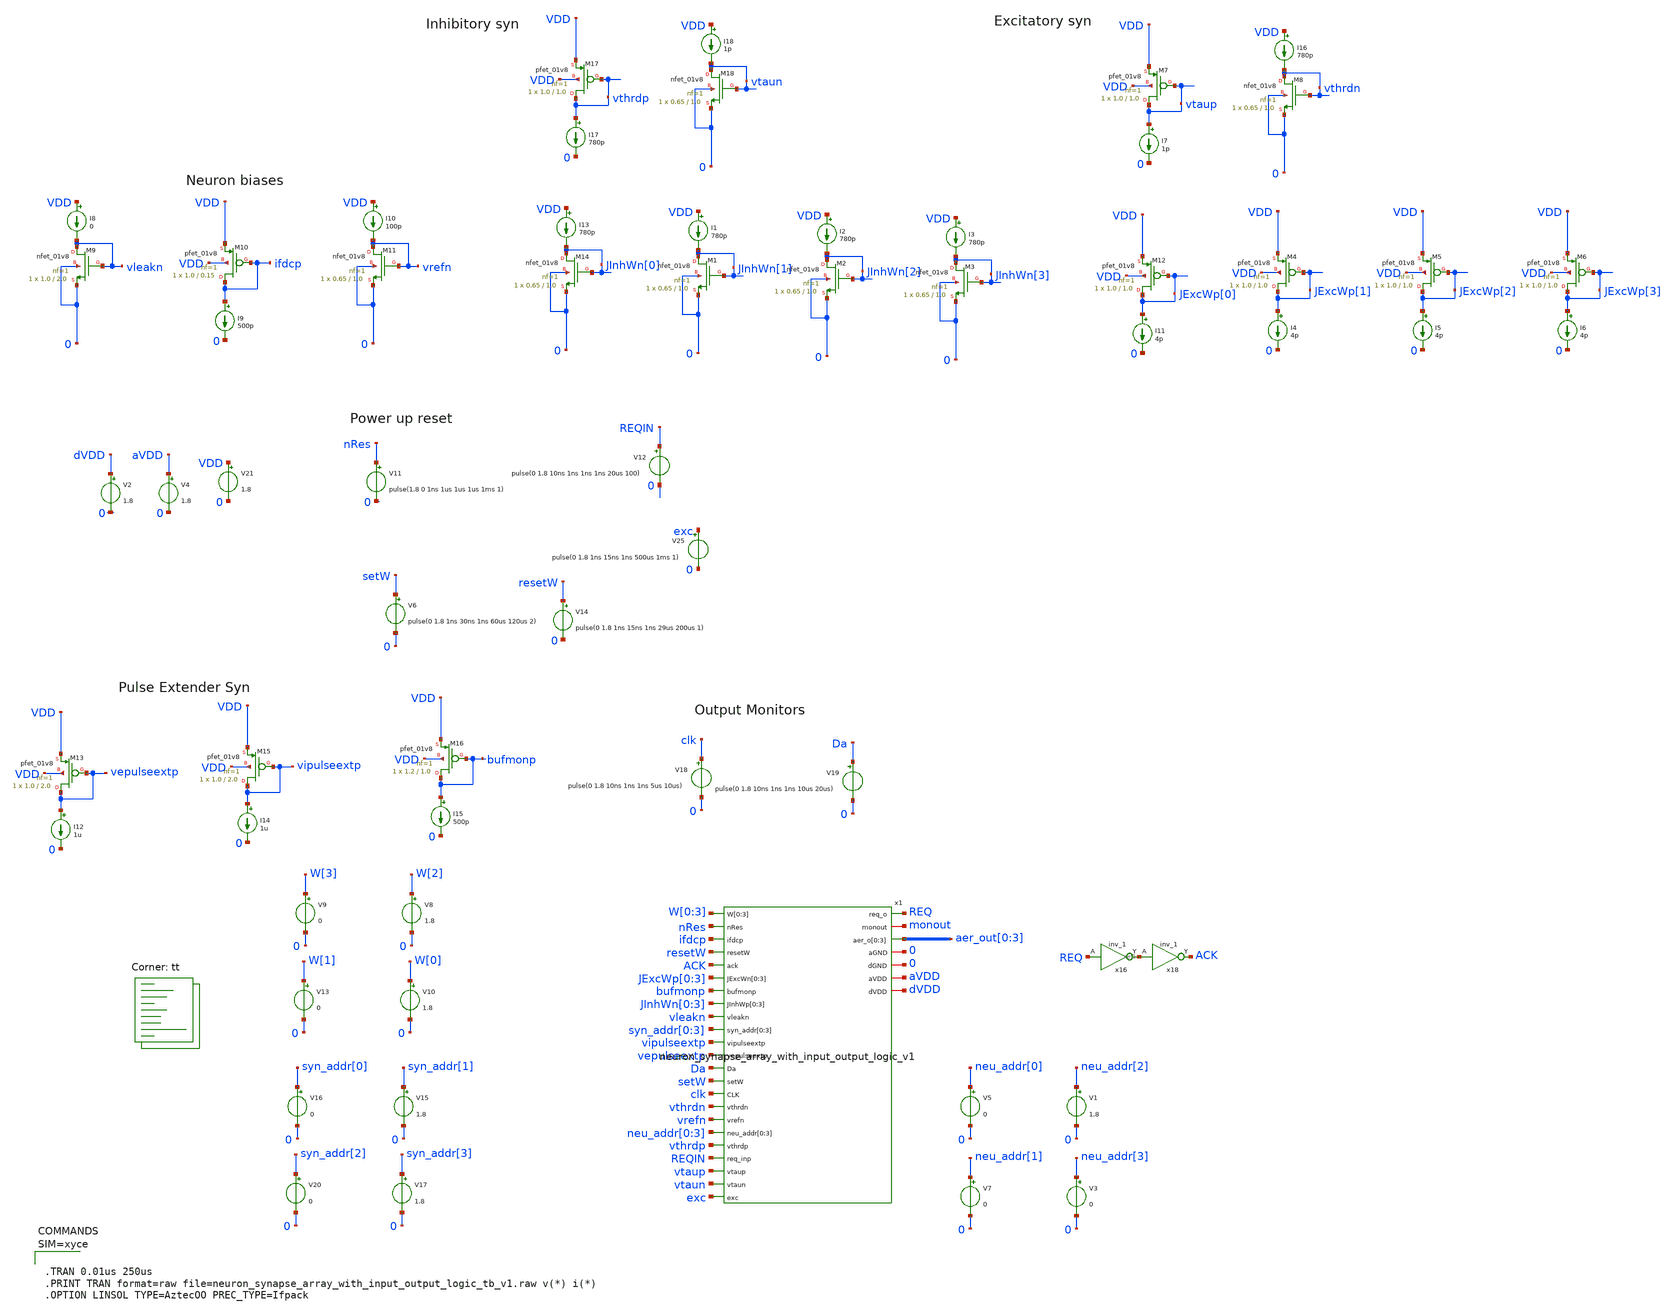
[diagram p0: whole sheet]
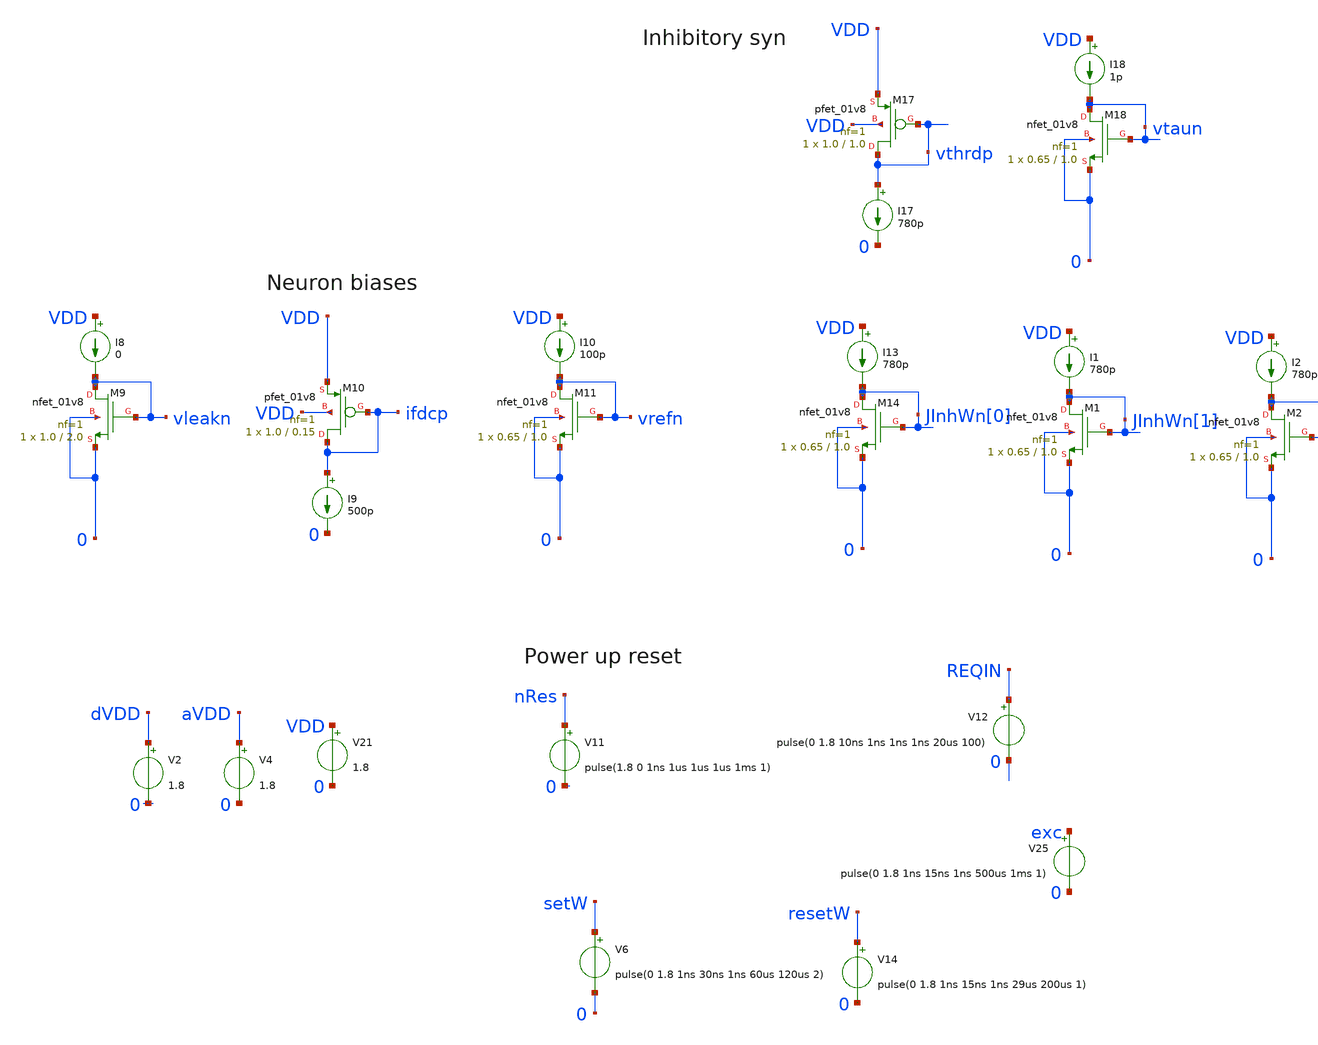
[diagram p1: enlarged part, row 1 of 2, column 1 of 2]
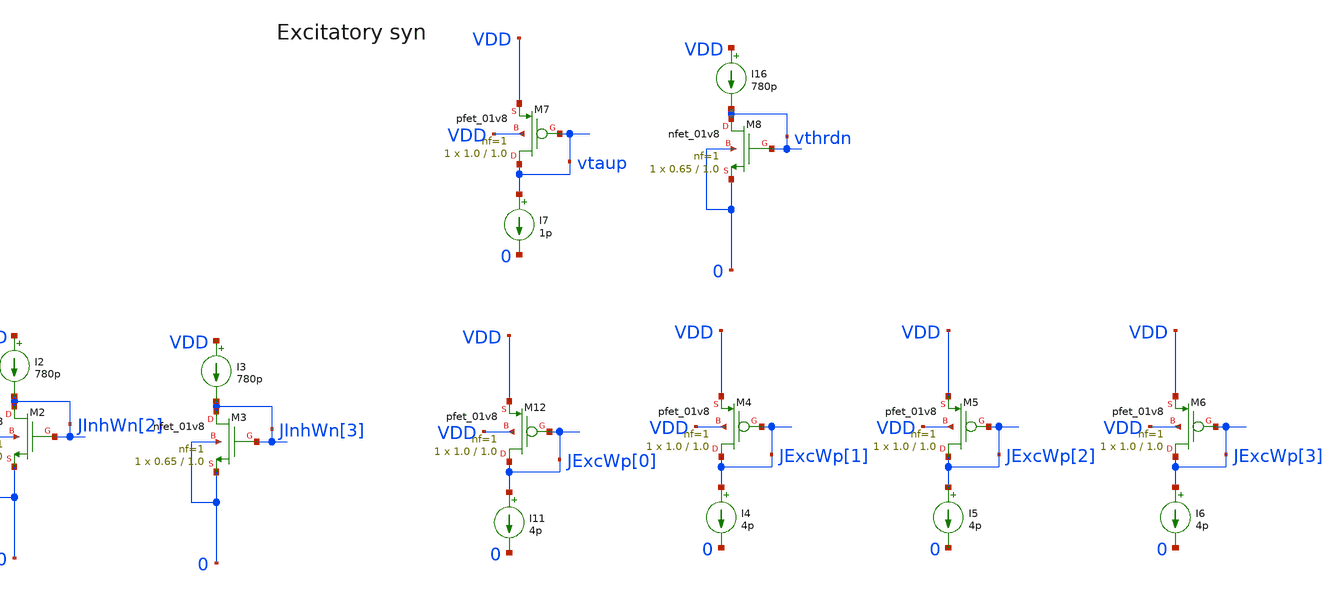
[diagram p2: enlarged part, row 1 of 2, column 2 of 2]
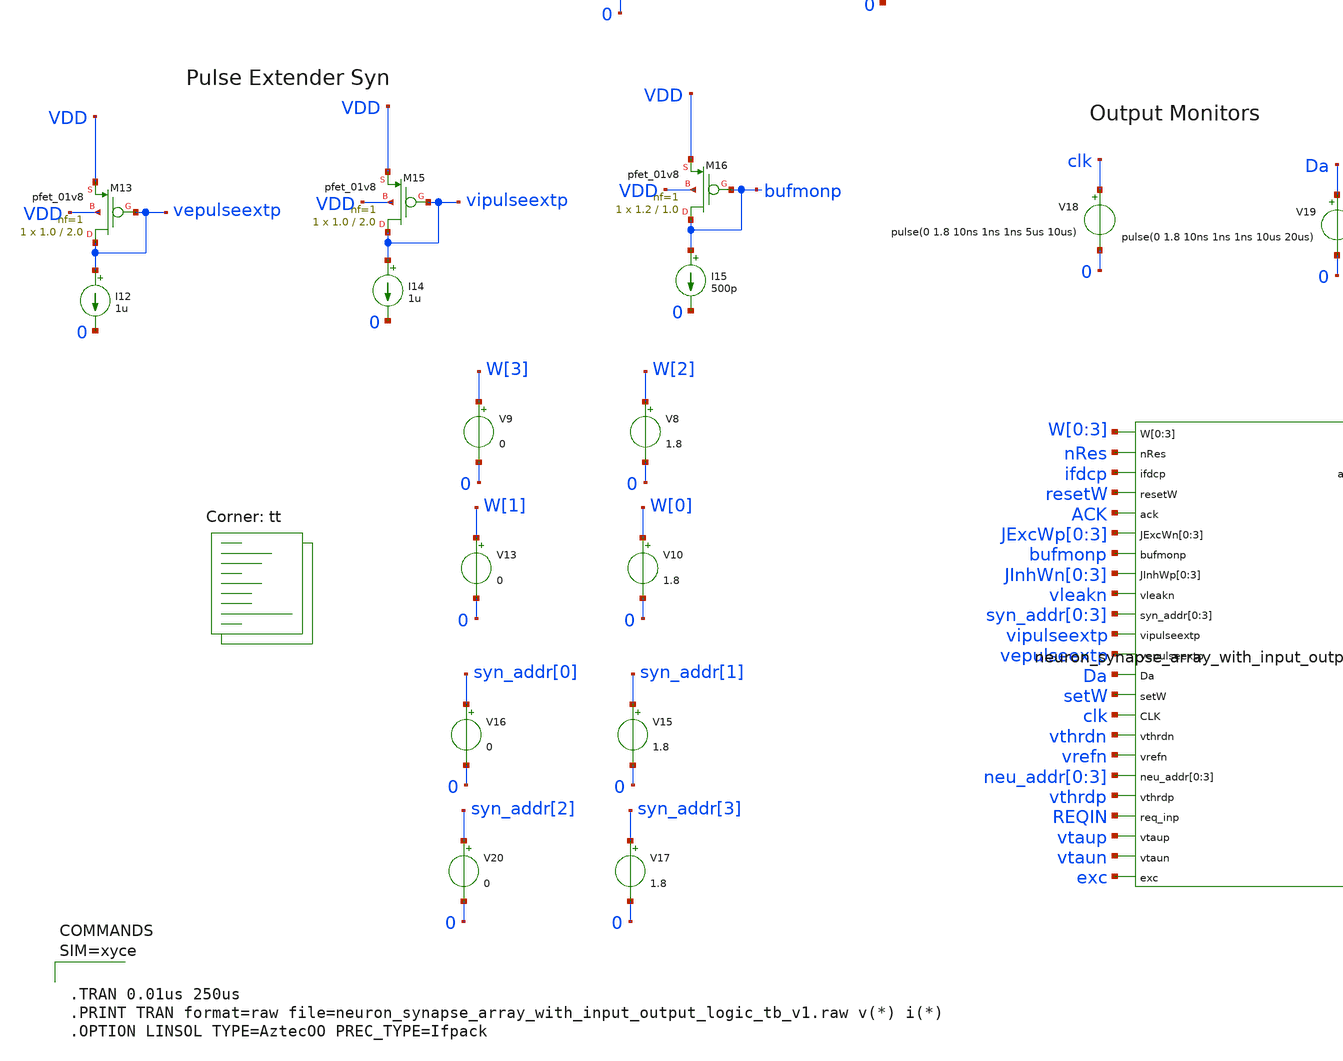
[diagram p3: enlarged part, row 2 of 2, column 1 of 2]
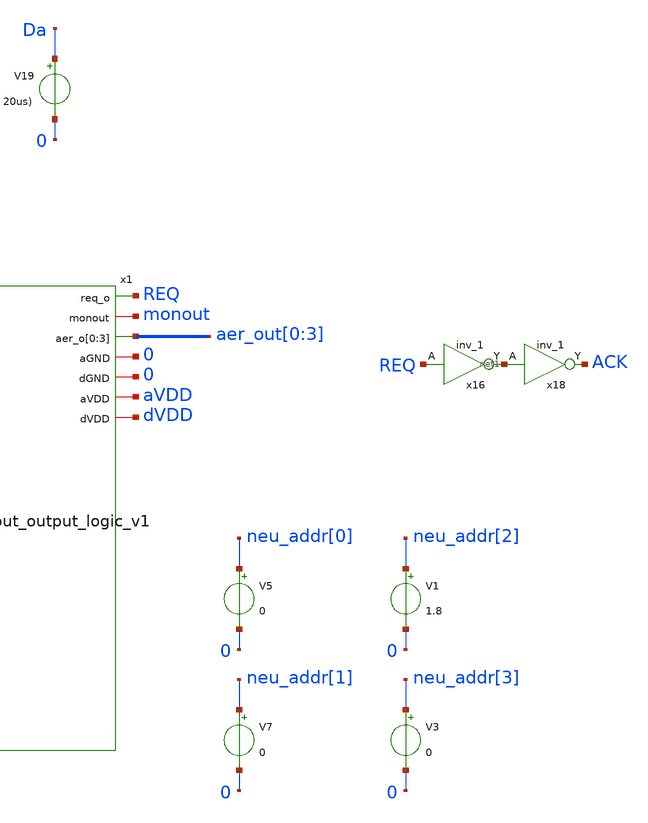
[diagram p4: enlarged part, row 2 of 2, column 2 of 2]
** sch_path: design/xschem/neuron_synapse_array_with_input_output_logic_v1_tb.sch
**.subckt neuron_synapse_array_with_input_output_logic_v1_tb
V2 dVDD 0 1.8
V12 REQIN 0 pulse(0 1.8 10ns 1ns 1ns 1ns 20us 100)
V4 aVDD 0 1.8
V11 nRes 0 pulse(1.8 0 1ns 1us 1us 1us 1ms 1)
V6 setW 0 pulse(0 1.8 1ns 30ns 1ns 60us 120us 2)
V14 resetW 0 pulse(0 1.8 1ns 15ns 1ns 29us 200us 1)
V25 exc 0 pulse(0 1.8 1ns 15ns 1ns 500us 1ms 1)
x16 REQ 0 0 dVDD dVDD net1 sky130_fd_sc_hd__inv_1
x18 net1 0 0 dVDD dVDD ACK sky130_fd_sc_hd__inv_1
x1 W[0] W[1] W[2] W[3] REQ monout nRes aer_out[0] aer_out[1] aer_out[2] aer_out[3] ifdcp resetW ACK
+ JExcWp[0] JExcWp[1] JExcWp[2] JExcWp[3] bufmonp JInhWn[0] JInhWn[1] JInhWn[2] JInhWn[3] vleakn syn_addr[0]
+ syn_addr[1] syn_addr[2] syn_addr[3] vipulseextp vepulseextp Da setW clk vthrdn vrefn neu_addr[0] neu_addr[1]
+ neu_addr[2] neu_addr[3] vthrdp REQIN vtaup vtaun exc 0 0 aVDD dVDD
+ neuron_synapse_array_with_input_output_logic_v1
V21 VDD 0 1.8
I8 VDD vleakn 0
XM9 vleakn vleakn 0 0 sky130_fd_pr__nfet_01v8 L=2.0 W=1.0 nf=1 ad='int((nf+1)/2) * W/nf * 0.29' as='int((nf+2)/2) * W/nf * 0.29'
+ pd='2*int((nf+1)/2) * (W/nf + 0.29)' ps='2*int((nf+2)/2) * (W/nf + 0.29)' nrd='0.29 / W' nrs='0.29 / W'
+ sa=0 sb=0 sd=0 mult=1 m=1
XM10 ifdcp ifdcp VDD VDD sky130_fd_pr__pfet_01v8 L=0.15 W=1.0 nf=1 ad='int((nf+1)/2) * W/nf * 0.29' as='int((nf+2)/2) * W/nf * 0.29'
+ pd='2*int((nf+1)/2) * (W/nf + 0.29)' ps='2*int((nf+2)/2) * (W/nf + 0.29)' nrd='0.29 / W' nrs='0.29 / W'
+ sa=0 sb=0 sd=0 mult=1 m=1
I9 ifdcp 0 500p
I10 VDD vrefn 100p
XM11 vrefn vrefn 0 0 sky130_fd_pr__nfet_01v8 L=1.0 W=0.65 nf=1 ad='int((nf+1)/2) * W/nf * 0.29' as='int((nf+2)/2) * W/nf * 0.29'
+ pd='2*int((nf+1)/2) * (W/nf + 0.29)' ps='2*int((nf+2)/2) * (W/nf + 0.29)' nrd='0.29 / W' nrs='0.29 / W'
+ sa=0 sb=0 sd=0 mult=1 m=1
I13 VDD JInhWn[0] 780p
XM14 JInhWn[0] JInhWn[0] 0 0 sky130_fd_pr__nfet_01v8 L=1.0 W=0.65 nf=1 ad='int((nf+1)/2) * W/nf * 0.29'
+ as='int((nf+2)/2) * W/nf * 0.29' pd='2*int((nf+1)/2) * (W/nf + 0.29)' ps='2*int((nf+2)/2) * (W/nf + 0.29)'
+ nrd='0.29 / W' nrs='0.29 / W' sa=0 sb=0 sd=0 mult=1 m=1
I1 VDD JInhWn[1] 780p
XM1 JInhWn[1] JInhWn[1] 0 0 sky130_fd_pr__nfet_01v8 L=1.0 W=0.65 nf=1 ad='int((nf+1)/2) * W/nf * 0.29'
+ as='int((nf+2)/2) * W/nf * 0.29' pd='2*int((nf+1)/2) * (W/nf + 0.29)' ps='2*int((nf+2)/2) * (W/nf + 0.29)'
+ nrd='0.29 / W' nrs='0.29 / W' sa=0 sb=0 sd=0 mult=1 m=1
I2 VDD JInhWn[2] 780p
XM2 JInhWn[2] JInhWn[2] 0 0 sky130_fd_pr__nfet_01v8 L=1.0 W=0.65 nf=1 ad='int((nf+1)/2) * W/nf * 0.29'
+ as='int((nf+2)/2) * W/nf * 0.29' pd='2*int((nf+1)/2) * (W/nf + 0.29)' ps='2*int((nf+2)/2) * (W/nf + 0.29)'
+ nrd='0.29 / W' nrs='0.29 / W' sa=0 sb=0 sd=0 mult=1 m=1
I3 VDD JInhWn[3] 780p
XM3 JInhWn[3] JInhWn[3] 0 0 sky130_fd_pr__nfet_01v8 L=1.0 W=0.65 nf=1 ad='int((nf+1)/2) * W/nf * 0.29'
+ as='int((nf+2)/2) * W/nf * 0.29' pd='2*int((nf+1)/2) * (W/nf + 0.29)' ps='2*int((nf+2)/2) * (W/nf + 0.29)'
+ nrd='0.29 / W' nrs='0.29 / W' sa=0 sb=0 sd=0 mult=1 m=1
XM12 JExcWp[0] JExcWp[0] VDD VDD sky130_fd_pr__pfet_01v8 L=1.0 W=1.0 nf=1 ad='int((nf+1)/2) * W/nf * 0.29'
+ as='int((nf+2)/2) * W/nf * 0.29' pd='2*int((nf+1)/2) * (W/nf + 0.29)' ps='2*int((nf+2)/2) * (W/nf + 0.29)'
+ nrd='0.29 / W' nrs='0.29 / W' sa=0 sb=0 sd=0 mult=1 m=1
I11 JExcWp[0] 0 4p
XM4 JExcWp[1] JExcWp[1] VDD VDD sky130_fd_pr__pfet_01v8 L=1.0 W=1.0 nf=1 ad='int((nf+1)/2) * W/nf * 0.29'
+ as='int((nf+2)/2) * W/nf * 0.29' pd='2*int((nf+1)/2) * (W/nf + 0.29)' ps='2*int((nf+2)/2) * (W/nf + 0.29)'
+ nrd='0.29 / W' nrs='0.29 / W' sa=0 sb=0 sd=0 mult=1 m=1
I4 JExcWp[1] 0 4p
XM5 JExcWp[2] JExcWp[2] VDD VDD sky130_fd_pr__pfet_01v8 L=1.0 W=1.0 nf=1 ad='int((nf+1)/2) * W/nf * 0.29'
+ as='int((nf+2)/2) * W/nf * 0.29' pd='2*int((nf+1)/2) * (W/nf + 0.29)' ps='2*int((nf+2)/2) * (W/nf + 0.29)'
+ nrd='0.29 / W' nrs='0.29 / W' sa=0 sb=0 sd=0 mult=1 m=1
I5 JExcWp[2] 0 4p
XM6 JExcWp[3] JExcWp[3] VDD VDD sky130_fd_pr__pfet_01v8 L=1.0 W=1.0 nf=1 ad='int((nf+1)/2) * W/nf * 0.29'
+ as='int((nf+2)/2) * W/nf * 0.29' pd='2*int((nf+1)/2) * (W/nf + 0.29)' ps='2*int((nf+2)/2) * (W/nf + 0.29)'
+ nrd='0.29 / W' nrs='0.29 / W' sa=0 sb=0 sd=0 mult=1 m=1
I6 JExcWp[3] 0 4p
XM13 vepulseextp vepulseextp VDD VDD sky130_fd_pr__pfet_01v8 L=2.0 W=1.0 nf=1 ad='int((nf+1)/2) * W/nf * 0.29'
+ as='int((nf+2)/2) * W/nf * 0.29' pd='2*int((nf+1)/2) * (W/nf + 0.29)' ps='2*int((nf+2)/2) * (W/nf + 0.29)'
+ nrd='0.29 / W' nrs='0.29 / W' sa=0 sb=0 sd=0 mult=1 m=1
I12 vepulseextp 0 1u
XM15 vipulseextp vipulseextp VDD VDD sky130_fd_pr__pfet_01v8 L=2.0 W=1.0 nf=1 ad='int((nf+1)/2) * W/nf * 0.29'
+ as='int((nf+2)/2) * W/nf * 0.29' pd='2*int((nf+1)/2) * (W/nf + 0.29)' ps='2*int((nf+2)/2) * (W/nf + 0.29)'
+ nrd='0.29 / W' nrs='0.29 / W' sa=0 sb=0 sd=0 mult=1 m=1
I14 vipulseextp 0 1u
XM16 bufmonp bufmonp VDD VDD sky130_fd_pr__pfet_01v8 L=1.0 W=1.2 nf=1 ad='int((nf+1)/2) * W/nf * 0.29'
+ as='int((nf+2)/2) * W/nf * 0.29' pd='2*int((nf+1)/2) * (W/nf + 0.29)' ps='2*int((nf+2)/2) * (W/nf + 0.29)'
+ nrd='0.29 / W' nrs='0.29 / W' sa=0 sb=0 sd=0 mult=1 m=1
I15 bufmonp 0 500p
XM7 vtaup vtaup VDD VDD sky130_fd_pr__pfet_01v8 L=1.0 W=1.0 nf=1 ad='int((nf+1)/2) * W/nf * 0.29' as='int((nf+2)/2) * W/nf * 0.29'
+ pd='2*int((nf+1)/2) * (W/nf + 0.29)' ps='2*int((nf+2)/2) * (W/nf + 0.29)' nrd='0.29 / W' nrs='0.29 / W'
+ sa=0 sb=0 sd=0 mult=1 m=1
I7 vtaup 0 1p
I16 VDD vthrdn 780p
XM8 vthrdn vthrdn 0 0 sky130_fd_pr__nfet_01v8 L=1.0 W=0.65 nf=1 ad='int((nf+1)/2) * W/nf * 0.29' as='int((nf+2)/2) * W/nf * 0.29'
+ pd='2*int((nf+1)/2) * (W/nf + 0.29)' ps='2*int((nf+2)/2) * (W/nf + 0.29)' nrd='0.29 / W' nrs='0.29 / W'
+ sa=0 sb=0 sd=0 mult=1 m=1
XM17 vthrdp vthrdp VDD VDD sky130_fd_pr__pfet_01v8 L=1.0 W=1.0 nf=1 ad='int((nf+1)/2) * W/nf * 0.29'
+ as='int((nf+2)/2) * W/nf * 0.29' pd='2*int((nf+1)/2) * (W/nf + 0.29)' ps='2*int((nf+2)/2) * (W/nf + 0.29)'
+ nrd='0.29 / W' nrs='0.29 / W' sa=0 sb=0 sd=0 mult=1 m=1
I17 vthrdp 0 780p
I18 VDD vtaun 1p
XM18 vtaun vtaun 0 0 sky130_fd_pr__nfet_01v8 L=1.0 W=0.65 nf=1 ad='int((nf+1)/2) * W/nf * 0.29' as='int((nf+2)/2) * W/nf * 0.29'
+ pd='2*int((nf+1)/2) * (W/nf + 0.29)' ps='2*int((nf+2)/2) * (W/nf + 0.29)' nrd='0.29 / W' nrs='0.29 / W'
+ sa=0 sb=0 sd=0 mult=1 m=1
V18 clk 0 pulse(0 1.8 10ns 1ns 1ns 5us 10us)
V19 Da 0 pulse(0 1.8 10ns 1ns 1ns 10us 20us)
V1 neu_addr[2] 0 1.8
V3 neu_addr[3] 0 0
V5 neu_addr[0] 0 0
V7 neu_addr[1] 0 0
V8 W[2] 0 1.8
V9 W[3] 0 0
V10 W[0] 0 1.8
V13 W[1] 0 0
V15 syn_addr[1] 0 1.8
V16 syn_addr[0] 0 0
V17 syn_addr[3] 0 1.8
V20 syn_addr[2] 0 0
**** begin user architecture code


* Standard cell simulation files
.include $::SKYWATER_STDCELLS/sky130_fd_sc_hd.spice


.lib $::SKYWATER_MODELS/sky130.lib.spice tt



**** end user architecture code
**.ends
.end
